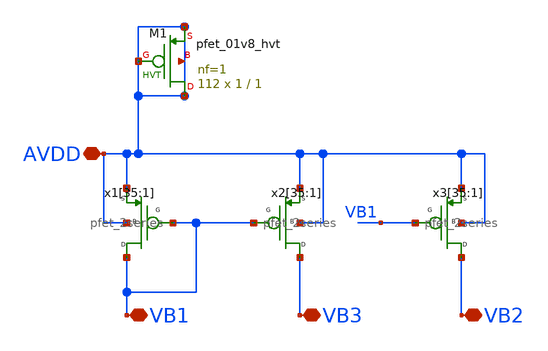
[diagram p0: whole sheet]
** sch_path: xschem/INA_layout_v2/bias/pbias_vb123.sch
**.subckt pbias_vb123 VB1 VB2 VB3 AVDD
*.iopin VB1
*.iopin VB2
*.iopin VB3
*.iopin AVDD
x1[35] AVDD AVDD VB1 VB1 pfet_2series
x1[34] AVDD AVDD VB1 VB1 pfet_2series
x1[33] AVDD AVDD VB1 VB1 pfet_2series
x1[32] AVDD AVDD VB1 VB1 pfet_2series
x1[31] AVDD AVDD VB1 VB1 pfet_2series
x1[30] AVDD AVDD VB1 VB1 pfet_2series
x1[29] AVDD AVDD VB1 VB1 pfet_2series
x1[28] AVDD AVDD VB1 VB1 pfet_2series
x1[27] AVDD AVDD VB1 VB1 pfet_2series
x1[26] AVDD AVDD VB1 VB1 pfet_2series
x1[25] AVDD AVDD VB1 VB1 pfet_2series
x1[24] AVDD AVDD VB1 VB1 pfet_2series
x1[23] AVDD AVDD VB1 VB1 pfet_2series
x1[22] AVDD AVDD VB1 VB1 pfet_2series
x1[21] AVDD AVDD VB1 VB1 pfet_2series
x1[20] AVDD AVDD VB1 VB1 pfet_2series
x1[19] AVDD AVDD VB1 VB1 pfet_2series
x1[18] AVDD AVDD VB1 VB1 pfet_2series
x1[17] AVDD AVDD VB1 VB1 pfet_2series
x1[16] AVDD AVDD VB1 VB1 pfet_2series
x1[15] AVDD AVDD VB1 VB1 pfet_2series
x1[14] AVDD AVDD VB1 VB1 pfet_2series
x1[13] AVDD AVDD VB1 VB1 pfet_2series
x1[12] AVDD AVDD VB1 VB1 pfet_2series
x1[11] AVDD AVDD VB1 VB1 pfet_2series
x1[10] AVDD AVDD VB1 VB1 pfet_2series
x1[9] AVDD AVDD VB1 VB1 pfet_2series
x1[8] AVDD AVDD VB1 VB1 pfet_2series
x1[7] AVDD AVDD VB1 VB1 pfet_2series
x1[6] AVDD AVDD VB1 VB1 pfet_2series
x1[5] AVDD AVDD VB1 VB1 pfet_2series
x1[4] AVDD AVDD VB1 VB1 pfet_2series
x1[3] AVDD AVDD VB1 VB1 pfet_2series
x1[2] AVDD AVDD VB1 VB1 pfet_2series
x1[1] AVDD AVDD VB1 VB1 pfet_2series
x2[35] AVDD AVDD VB1 VB3 pfet_2series
x2[34] AVDD AVDD VB1 VB3 pfet_2series
x2[33] AVDD AVDD VB1 VB3 pfet_2series
x2[32] AVDD AVDD VB1 VB3 pfet_2series
x2[31] AVDD AVDD VB1 VB3 pfet_2series
x2[30] AVDD AVDD VB1 VB3 pfet_2series
x2[29] AVDD AVDD VB1 VB3 pfet_2series
x2[28] AVDD AVDD VB1 VB3 pfet_2series
x2[27] AVDD AVDD VB1 VB3 pfet_2series
x2[26] AVDD AVDD VB1 VB3 pfet_2series
x2[25] AVDD AVDD VB1 VB3 pfet_2series
x2[24] AVDD AVDD VB1 VB3 pfet_2series
x2[23] AVDD AVDD VB1 VB3 pfet_2series
x2[22] AVDD AVDD VB1 VB3 pfet_2series
x2[21] AVDD AVDD VB1 VB3 pfet_2series
x2[20] AVDD AVDD VB1 VB3 pfet_2series
x2[19] AVDD AVDD VB1 VB3 pfet_2series
x2[18] AVDD AVDD VB1 VB3 pfet_2series
x2[17] AVDD AVDD VB1 VB3 pfet_2series
x2[16] AVDD AVDD VB1 VB3 pfet_2series
x2[15] AVDD AVDD VB1 VB3 pfet_2series
x2[14] AVDD AVDD VB1 VB3 pfet_2series
x2[13] AVDD AVDD VB1 VB3 pfet_2series
x2[12] AVDD AVDD VB1 VB3 pfet_2series
x2[11] AVDD AVDD VB1 VB3 pfet_2series
x2[10] AVDD AVDD VB1 VB3 pfet_2series
x2[9] AVDD AVDD VB1 VB3 pfet_2series
x2[8] AVDD AVDD VB1 VB3 pfet_2series
x2[7] AVDD AVDD VB1 VB3 pfet_2series
x2[6] AVDD AVDD VB1 VB3 pfet_2series
x2[5] AVDD AVDD VB1 VB3 pfet_2series
x2[4] AVDD AVDD VB1 VB3 pfet_2series
x2[3] AVDD AVDD VB1 VB3 pfet_2series
x2[2] AVDD AVDD VB1 VB3 pfet_2series
x2[1] AVDD AVDD VB1 VB3 pfet_2series
x3[35] AVDD AVDD VB1 VB2 pfet_2series
x3[34] AVDD AVDD VB1 VB2 pfet_2series
x3[33] AVDD AVDD VB1 VB2 pfet_2series
x3[32] AVDD AVDD VB1 VB2 pfet_2series
x3[31] AVDD AVDD VB1 VB2 pfet_2series
x3[30] AVDD AVDD VB1 VB2 pfet_2series
x3[29] AVDD AVDD VB1 VB2 pfet_2series
x3[28] AVDD AVDD VB1 VB2 pfet_2series
x3[27] AVDD AVDD VB1 VB2 pfet_2series
x3[26] AVDD AVDD VB1 VB2 pfet_2series
x3[25] AVDD AVDD VB1 VB2 pfet_2series
x3[24] AVDD AVDD VB1 VB2 pfet_2series
x3[23] AVDD AVDD VB1 VB2 pfet_2series
x3[22] AVDD AVDD VB1 VB2 pfet_2series
x3[21] AVDD AVDD VB1 VB2 pfet_2series
x3[20] AVDD AVDD VB1 VB2 pfet_2series
x3[19] AVDD AVDD VB1 VB2 pfet_2series
x3[18] AVDD AVDD VB1 VB2 pfet_2series
x3[17] AVDD AVDD VB1 VB2 pfet_2series
x3[16] AVDD AVDD VB1 VB2 pfet_2series
x3[15] AVDD AVDD VB1 VB2 pfet_2series
x3[14] AVDD AVDD VB1 VB2 pfet_2series
x3[13] AVDD AVDD VB1 VB2 pfet_2series
x3[12] AVDD AVDD VB1 VB2 pfet_2series
x3[11] AVDD AVDD VB1 VB2 pfet_2series
x3[10] AVDD AVDD VB1 VB2 pfet_2series
x3[9] AVDD AVDD VB1 VB2 pfet_2series
x3[8] AVDD AVDD VB1 VB2 pfet_2series
x3[7] AVDD AVDD VB1 VB2 pfet_2series
x3[6] AVDD AVDD VB1 VB2 pfet_2series
x3[5] AVDD AVDD VB1 VB2 pfet_2series
x3[4] AVDD AVDD VB1 VB2 pfet_2series
x3[3] AVDD AVDD VB1 VB2 pfet_2series
x3[2] AVDD AVDD VB1 VB2 pfet_2series
x3[1] AVDD AVDD VB1 VB2 pfet_2series
XM1 AVDD AVDD AVDD AVDD sky130_fd_pr__pfet_01v8_hvt L=1 W=1 nf=1 ad='int((nf+1)/2) * W/nf * 0.29' as='int((nf+2)/2) * W/nf * 0.29'
+ pd='2*int((nf+1)/2) * (W/nf + 0.29)' ps='2*int((nf+2)/2) * (W/nf + 0.29)' nrd='0.29 / W' nrs='0.29 / W'
+ sa=0 sb=0 sd=0 mult=112 m=112
**.ends

* expanding   symbol:  INA_layout_v2/bias/pfet_2series.sym # of pins=4
** sym_path: INA_layout_v2/bias/pfet_2series.sym
** sch_path: INA_layout_v2/bias/pfet_2series.sch
.subckt pfet_2series S B G D
*.iopin S
*.iopin B
*.iopin G
*.iopin D
XM1 net1 G S B sky130_fd_pr__pfet_01v8_hvt L=1 W=1 nf=1 ad='int((nf+1)/2) * W/nf * 0.29' as='int((nf+2)/2) * W/nf * 0.29'
+ pd='2*int((nf+1)/2) * (W/nf + 0.29)' ps='2*int((nf+2)/2) * (W/nf + 0.29)' nrd='0.29 / W' nrs='0.29 / W'
+ sa=0 sb=0 sd=0 mult=1 m=1
XM2 D G net1 B sky130_fd_pr__pfet_01v8_hvt L=1 W=1 nf=1 ad='int((nf+1)/2) * W/nf * 0.29' as='int((nf+2)/2) * W/nf * 0.29'
+ pd='2*int((nf+1)/2) * (W/nf + 0.29)' ps='2*int((nf+2)/2) * (W/nf + 0.29)' nrd='0.29 / W' nrs='0.29 / W'
+ sa=0 sb=0 sd=0 mult=1 m=1
.ends

.end
